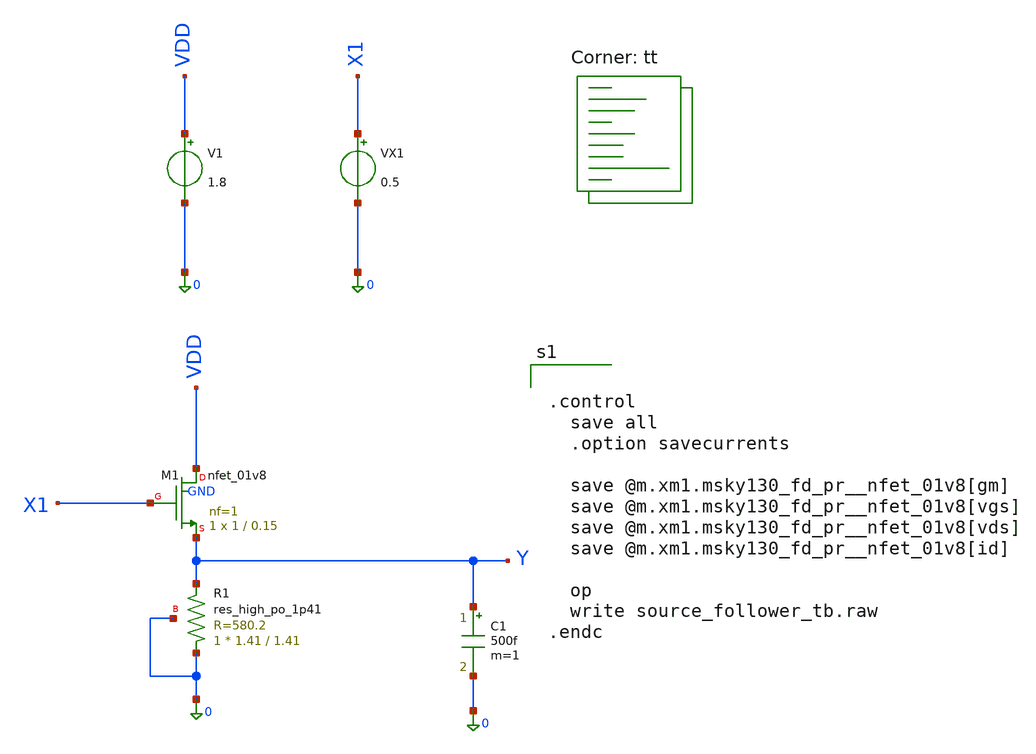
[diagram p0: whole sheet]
** sch_path: src/analog_source_files/source_follower_tb.sch
**.subckt source_follower_tb
C1 Y 0 500f m=1
V1 VDD 0 1.8
VX1 X1 0 0.5
XR1 0 Y 0 sky130_fd_pr__res_high_po_1p41 L=1.41 mult=1 m=1
XM1 VDD X1 Y GND sky130_fd_pr__nfet_01v8 L=0.15 W=1 nf=1 ad='int((1 + 1)/2) * 1 / 1 * 0.29' as='int((1 + 2)/2) * 1 / 1 * 0.29'
+ pd='2*int((1 + 1)/2) * (1 / 1 + 0.29)' ps='2*int((1 + 2)/2) * (1 / 1 + 0.29)' nrd='0.29 / 1 ' nrs='0.29 / 1 '
+ sa=0 sb=0 sd=0 mult=1 m=1
**** begin user architecture code
.lib $::SKYWATER_MODELS/sky130.lib.spice tt


.control
  save all
  .option savecurrents

  save @m.xm1.msky130_fd_pr__nfet_01v8[gm]
  save @m.xm1.msky130_fd_pr__nfet_01v8[vgs]
  save @m.xm1.msky130_fd_pr__nfet_01v8[vds]
  save @m.xm1.msky130_fd_pr__nfet_01v8[id]

  op
  write source_follower_tb.raw
.endc


**** end user architecture code
**.ends
.end
